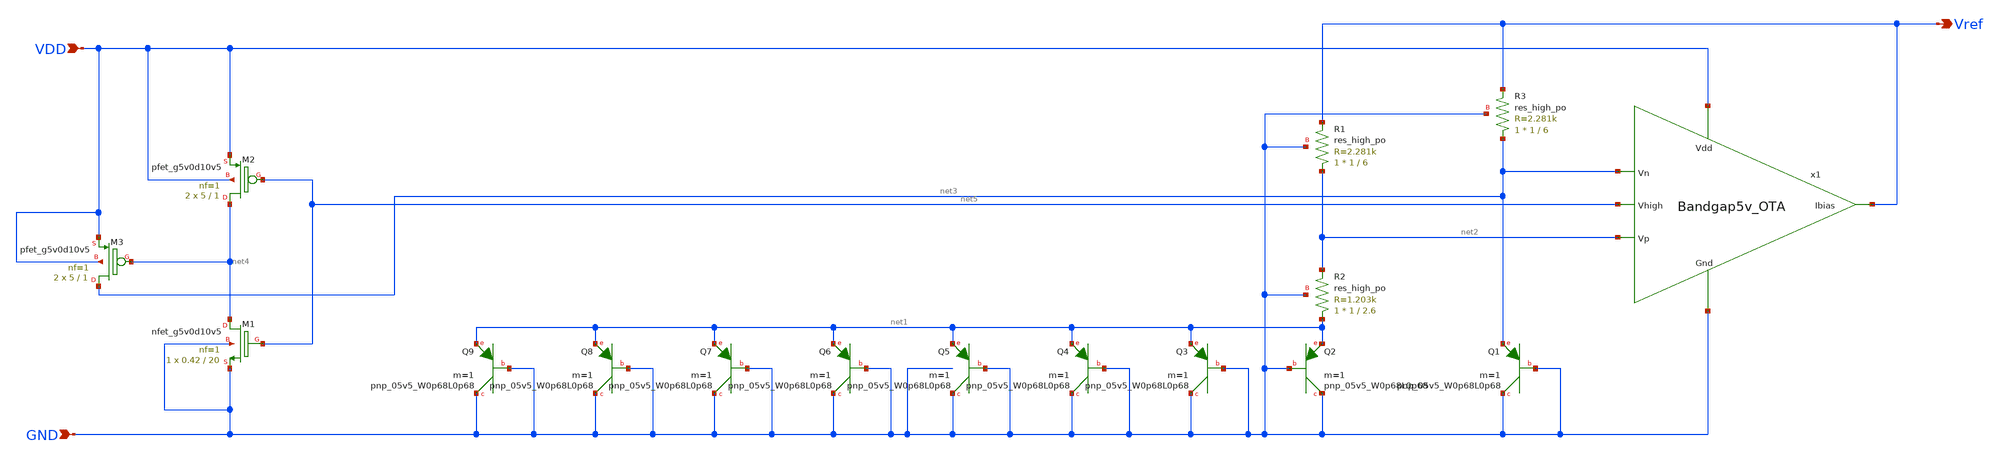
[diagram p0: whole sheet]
** sch_path: Analog_Blocks/LDO/Schematic/LDO_Miller_2.2v/Bandgap5v.sch
**.subckt Bandgap5v VDD GND Vref
*.ipin VDD
*.ipin GND
*.opin Vref
XQ1 GND GND net3 sky130_fd_pr__pnp_05v5_W0p68L0p68 m=1
XQ2 GND GND net1 sky130_fd_pr__pnp_05v5_W0p68L0p68 m=1
XQ3 GND GND net1 sky130_fd_pr__pnp_05v5_W0p68L0p68 m=1
XQ4 GND GND net1 sky130_fd_pr__pnp_05v5_W0p68L0p68 m=1
XQ5 GND GND net1 sky130_fd_pr__pnp_05v5_W0p68L0p68 m=1
XQ6 GND GND net1 sky130_fd_pr__pnp_05v5_W0p68L0p68 m=1
XQ7 GND GND net1 sky130_fd_pr__pnp_05v5_W0p68L0p68 m=1
XQ8 GND GND net1 sky130_fd_pr__pnp_05v5_W0p68L0p68 m=1
XQ9 GND GND net1 sky130_fd_pr__pnp_05v5_W0p68L0p68 m=1
XM2 net4 net5 VDD VDD sky130_fd_pr__pfet_g5v0d10v5 L=1 W=5 nf=1 ad='int((nf+1)/2) * W/nf * 0.29' as='int((nf+2)/2) * W/nf * 0.29'
+ pd='2*int((nf+1)/2) * (W/nf + 0.29)' ps='2*int((nf+2)/2) * (W/nf + 0.29)' nrd='0.29 / W' nrs='0.29 / W'
+ sa=0 sb=0 sd=0 mult=2 m=2
XM3 net3 net4 VDD VDD sky130_fd_pr__pfet_g5v0d10v5 L=1 W=5 nf=1 ad='int((nf+1)/2) * W/nf * 0.29' as='int((nf+2)/2) * W/nf * 0.29'
+ pd='2*int((nf+1)/2) * (W/nf + 0.29)' ps='2*int((nf+2)/2) * (W/nf + 0.29)' nrd='0.29 / W' nrs='0.29 / W'
+ sa=0 sb=0 sd=0 mult=2 m=2
XM1 net4 net5 GND GND sky130_fd_pr__nfet_g5v0d10v5 L=20 W=0.42 nf=1 ad='int((nf+1)/2) * W/nf * 0.29'
+ as='int((nf+2)/2) * W/nf * 0.29' pd='2*int((nf+1)/2) * (W/nf + 0.29)' ps='2*int((nf+2)/2) * (W/nf + 0.29)'
+ nrd='0.29 / W' nrs='0.29 / W' sa=0 sb=0 sd=0 mult=1 m=1
XR1 net2 Vref GND sky130_fd_pr__res_high_po W=1 L=6 mult=1 m=1
XR3 net3 Vref GND sky130_fd_pr__res_high_po W=1 L=6 mult=1 m=1
XR2 net1 net2 GND sky130_fd_pr__res_high_po W=1 L=2.6 mult=1 m=1
x1 VDD net3 net2 Vref net5 GND Bandgap5v_OTA
**.ends

* expanding   symbol:
*+  /home/eslam/mabrains/Analog_blocks/Analog_Blocks/LDO/Schematic/LDO_Miller_2.2v/Bandgap5v_OTA.sym # of pins=6
** sym_path: LDO/Schematic/Bandgap5v_OTA.sym
** sch_path: LDO/Schematic/Bandgap5v_OTA.sch
.subckt Bandgap5v_OTA Vdd Vn Vp Ibias Vhigh Gnd
*.opin Ibias
*.ipin Vhigh
*.ipin Vdd
*.ipin Gnd
*.ipin Vn
*.ipin Vp
XM6 Ibias Vhigh Vdd Vdd sky130_fd_pr__pfet_g5v0d10v5 L=1 W=10 nf=1 ad='int((nf+1)/2) * W/nf * 0.29' as='int((nf+2)/2) * W/nf * 0.29'
+ pd='2*int((nf+1)/2) * (W/nf + 0.29)' ps='2*int((nf+2)/2) * (W/nf + 0.29)' nrd='0.29 / W' nrs='0.29 / W'
+ sa=0 sb=0 sd=0 mult=1 m=1
XM5 net3 Vhigh Vdd Vdd sky130_fd_pr__pfet_g5v0d10v5 L=1 W=10 nf=1 ad='int((nf+1)/2) * W/nf * 0.29' as='int((nf+2)/2) * W/nf * 0.29'
+ pd='2*int((nf+1)/2) * (W/nf + 0.29)' ps='2*int((nf+2)/2) * (W/nf + 0.29)' nrd='0.29 / W' nrs='0.29 / W'
+ sa=0 sb=0 sd=0 mult=1 m=1
XM7 Vhigh Vhigh Vdd Vdd sky130_fd_pr__pfet_g5v0d10v5 L=1 W=54 nf=1 ad='int((nf+1)/2) * W/nf * 0.29' as='int((nf+2)/2) * W/nf * 0.29'
+ pd='2*int((nf+1)/2) * (W/nf + 0.29)' ps='2*int((nf+2)/2) * (W/nf + 0.29)' nrd='0.29 / W' nrs='0.29 / W'
+ sa=0 sb=0 sd=0 mult=1 m=1
XM2 net1 Vp net3 Vdd sky130_fd_pr__pfet_g5v0d10v5 L=1 W=30 nf=1 ad='int((nf+1)/2) * W/nf * 0.29' as='int((nf+2)/2) * W/nf * 0.29'
+ pd='2*int((nf+1)/2) * (W/nf + 0.29)' ps='2*int((nf+2)/2) * (W/nf + 0.29)' nrd='0.29 / W' nrs='0.29 / W'
+ sa=0 sb=0 sd=0 mult=1 m=1
XM1 net2 Vn net3 Vdd sky130_fd_pr__pfet_g5v0d10v5 L=1 W=30 nf=1 ad='int((nf+1)/2) * W/nf * 0.29' as='int((nf+2)/2) * W/nf * 0.29'
+ pd='2*int((nf+1)/2) * (W/nf + 0.29)' ps='2*int((nf+2)/2) * (W/nf + 0.29)' nrd='0.29 / W' nrs='0.29 / W'
+ sa=0 sb=0 sd=0 mult=1 m=1
XM8 Vhigh net1 Gnd Gnd sky130_fd_pr__nfet_g5v0d10v5 L=0.5 W=75 nf=1 ad='int((nf+1)/2) * W/nf * 0.29'
+ as='int((nf+2)/2) * W/nf * 0.29' pd='2*int((nf+1)/2) * (W/nf + 0.29)' ps='2*int((nf+2)/2) * (W/nf + 0.29)'
+ nrd='0.29 / W' nrs='0.29 / W' sa=0 sb=0 sd=0 mult=1 m=1
XM4 net1 net2 Gnd Gnd sky130_fd_pr__nfet_g5v0d10v5 L=0.5 W=7.5 nf=1 ad='int((nf+1)/2) * W/nf * 0.29'
+ as='int((nf+2)/2) * W/nf * 0.29' pd='2*int((nf+1)/2) * (W/nf + 0.29)' ps='2*int((nf+2)/2) * (W/nf + 0.29)'
+ nrd='0.29 / W' nrs='0.29 / W' sa=0 sb=0 sd=0 mult=1 m=1
XM3 net2 net2 Gnd Gnd sky130_fd_pr__nfet_g5v0d10v5 L=0.5 W=7.5 nf=1 ad='int((nf+1)/2) * W/nf * 0.29'
+ as='int((nf+2)/2) * W/nf * 0.29' pd='2*int((nf+1)/2) * (W/nf + 0.29)' ps='2*int((nf+2)/2) * (W/nf + 0.29)'
+ nrd='0.29 / W' nrs='0.29 / W' sa=0 sb=0 sd=0 mult=1 m=1
XC1 net1 Vhigh sky130_fd_pr__cap_mim_m3_2 W=1 L=1 MF=1 m=1
.ends

.end
